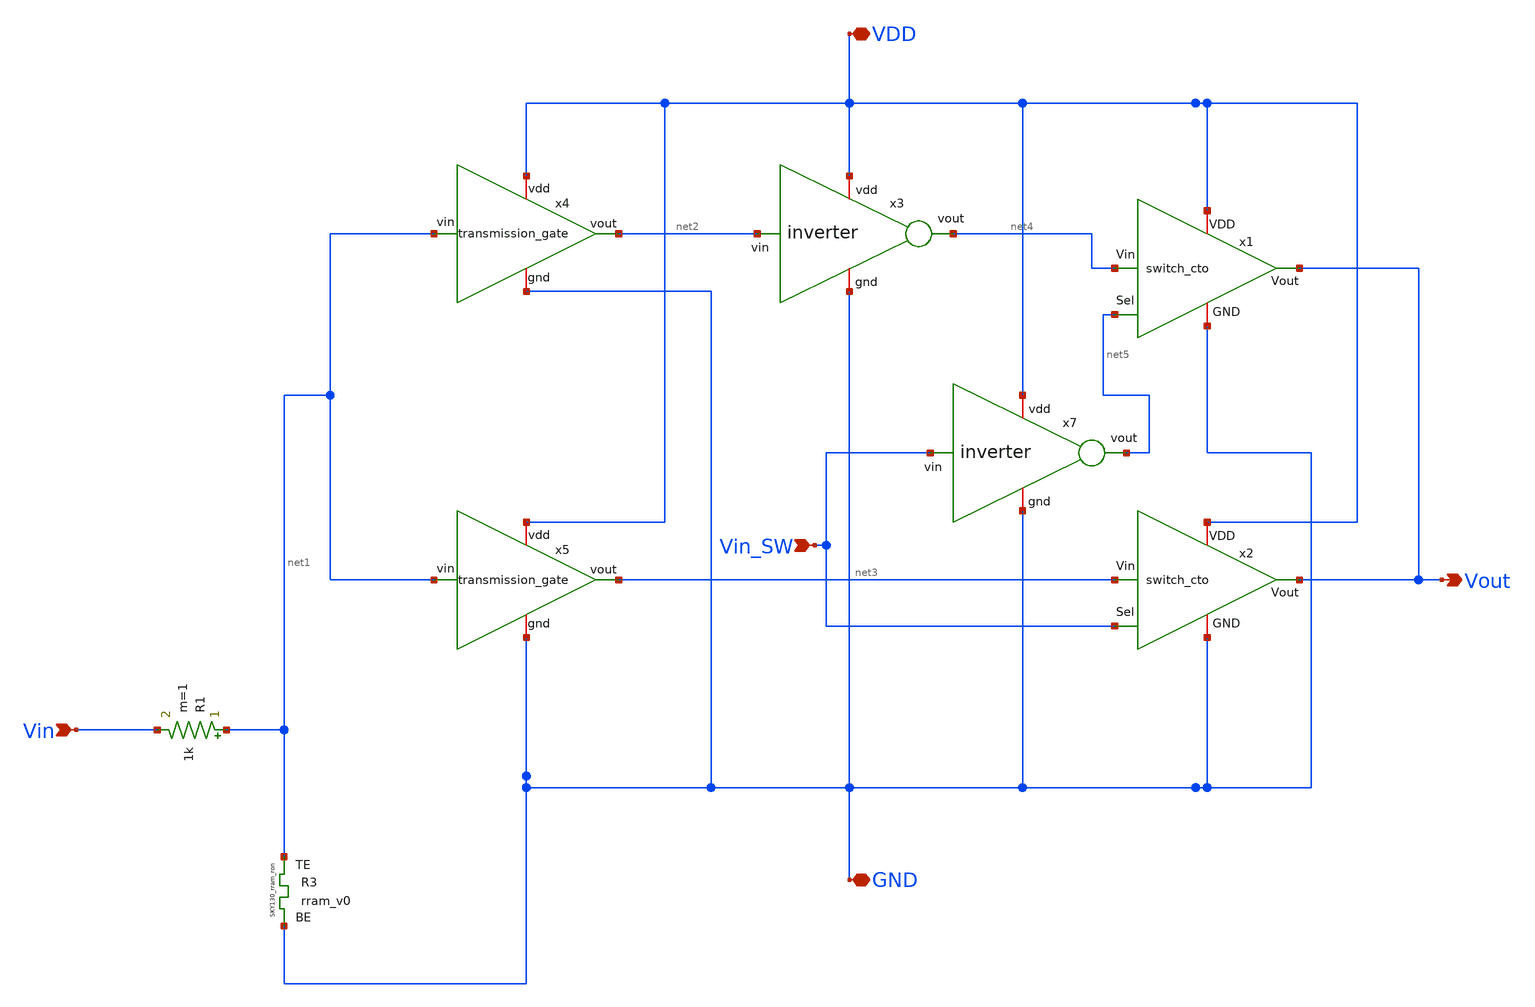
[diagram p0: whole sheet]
** sch_path: hopfield/sinapsis.sch
**.subckt sinapsis VDD Vin_SW Vin GND Vout
*.iopin VDD
*.ipin Vin_SW
*.ipin Vin
*.iopin GND
*.opin Vout
R1 net1 Vin 1k m=1
x3 VDD net4 net2 GND inverter
XR3 net1 GND rram_v0
x4 net1 GND VDD net2 transmission_gate
x5 net1 GND VDD net3 transmission_gate
x1 VDD GND net5 Vout net4 switch_cto
x2 VDD GND Vin_SW Vout net3 switch_cto
x7 VDD net5 Vin_SW GND inverter
**.ends
.end
